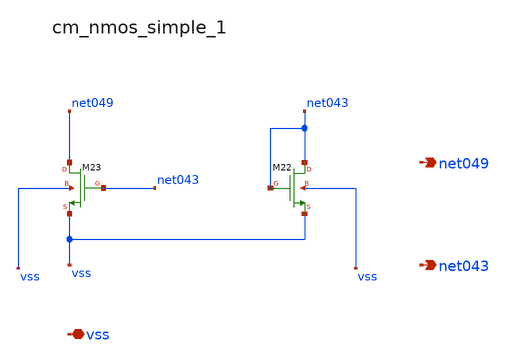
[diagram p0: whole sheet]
** sch_path: analog-db/raw/amp_005_hoilee_affc/hier/blocks/cm_nmos_simple_1.sch
**.subckt cm_nmos_simple_1 vss net049 net043
*.iopin vss
*.opin net049
*.opin net043
XM22 net043 net043 vss vss sg13_lv_nmos w=x_dut_xm22_w l=x_dut_xm22_l ng=1 m=x_dut_xm22_m
XM23 net049 net043 vss vss sg13_lv_nmos w=x_dut_xm23_w l=x_dut_xm23_l ng=1 m=x_dut_xm23_m
**.ends
.end
